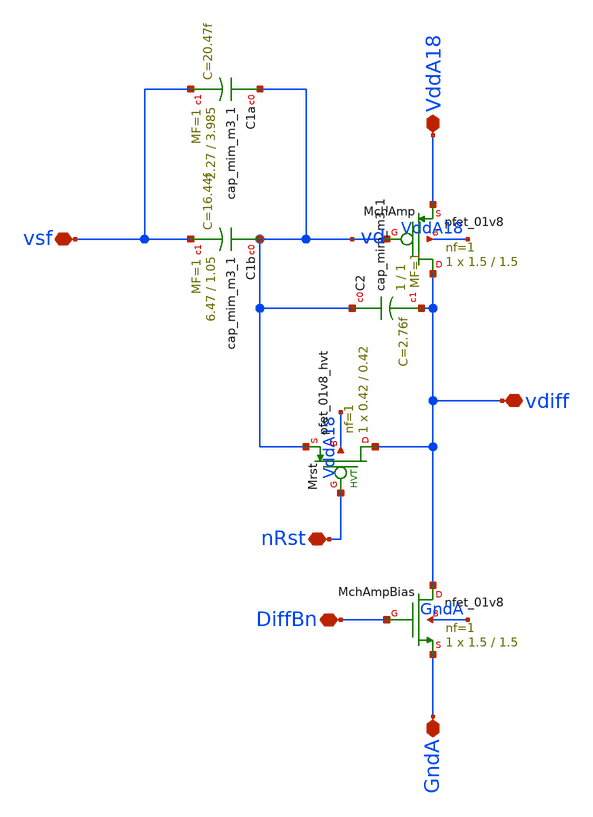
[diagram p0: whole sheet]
** sch_path: analog/klayout/production/final_merge_20260923/testbenches/cace/analog/xschem/PixelChangeAmplifier.sch
**.subckt PixelChangeAmplifier DiffBn vsf VddA18 GndA vdiff nRst
*.iopin DiffBn
*.iopin vsf
*.iopin VddA18
*.iopin GndA
*.iopin vdiff
*.iopin nRst
XC1b vd vsf sky130_fd_pr__cap_mim_m3_1 W=6.47 L=1.05 MF=1 m=1
XC2 vd vdiff sky130_fd_pr__cap_mim_m3_1 W=1 L=1 MF=1 m=1
XMchAmpBias vdiff DiffBn GndA GndA sky130_fd_pr__nfet_01v8 L=1.5 W=1.5 nf=1 ad='int((1 + 1)/2) * 1.5 / 1 * 0.29'
+ as='int((1 + 2)/2) * 1.5 / 1 * 0.29' pd='2*int((1 + 1)/2) * (1.5 / 1 + 0.29)' ps='2*int((1 + 2)/2) * (1.5 / 1 + 0.29)'
+ nrd='0.29 / 1.5 ' nrs='0.29 / 1.5 ' sa=0 sb=0 sd=0 mult=1 m=1
XMrst vdiff nRst vd VddA18 sky130_fd_pr__pfet_01v8_hvt L=0.42 W=0.42 nf=1 ad='int((1 + 1)/2) * 0.42 / 1 * 0.29'
+ as='int((1 + 2)/2) * 0.42 / 1 * 0.29' pd='2*int((1 + 1)/2) * (0.42 / 1 + 0.29)' ps='2*int((1 + 2)/2) * (0.42 / 1 + 0.29)'
+ nrd='0.29 / 0.42 ' nrs='0.29 / 0.42 ' sa=0 sb=0 sd=0 mult=1 m=1
XMchAmp vdiff vd VddA18 VddA18 sky130_fd_pr__pfet_01v8 L=1.5 W=1.5 nf=1 ad='int((1 + 1)/2) * 1.5 / 1 * 0.29'
+ as='int((1 + 2)/2) * 1.5 / 1 * 0.29' pd='2*int((1 + 1)/2) * (1.5 / 1 + 0.29)' ps='2*int((1 + 2)/2) * (1.5 / 1 + 0.29)'
+ nrd='0.29 / 1.5 ' nrs='0.29 / 1.5 ' sa=0 sb=0 sd=0 mult=1 m=1
XC1a vd vsf sky130_fd_pr__cap_mim_m3_1 W=2.27 L=3.985 MF=1 m=1
**.ends
.end
